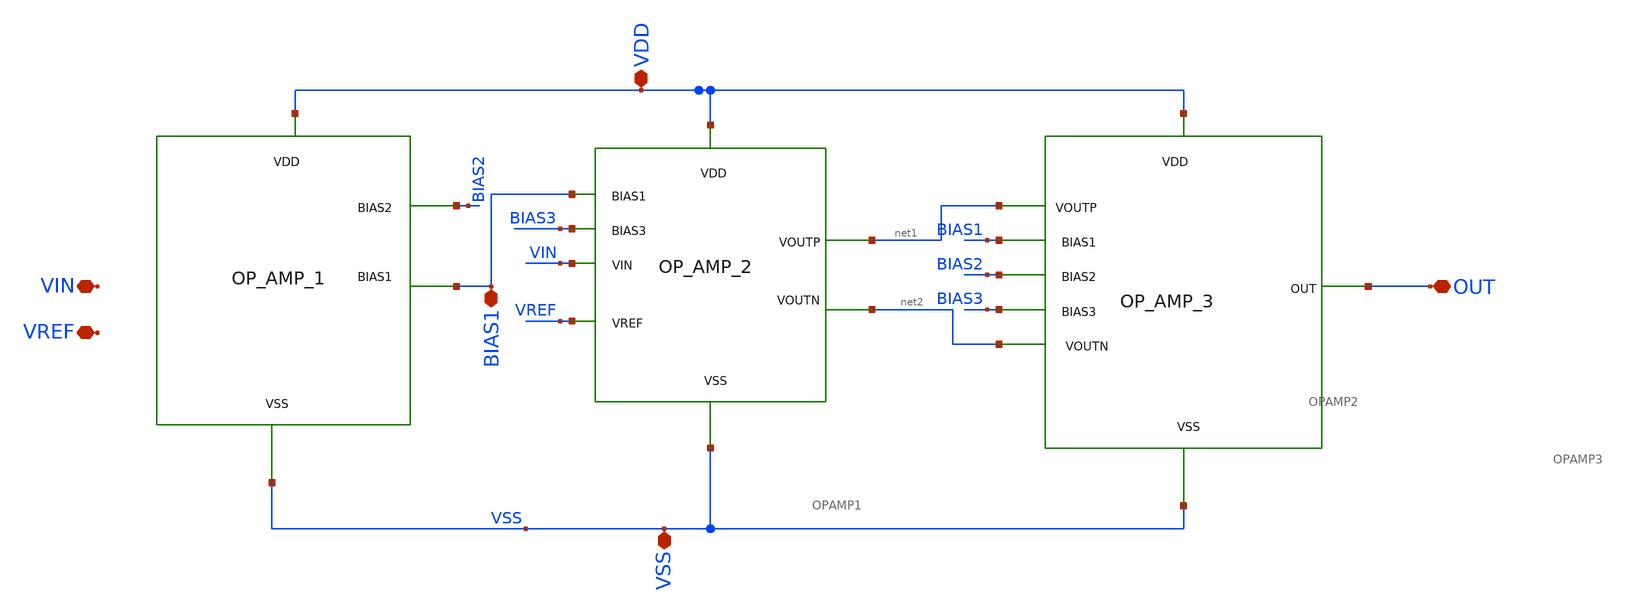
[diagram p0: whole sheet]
** sch_path: xschem/DC_DC_Converter_xschem/OPAMP_Blocks.sch
**.subckt OPAMP_Blocks VDD VSS BIAS1 VIN OUT VREF
*.iopin VDD
*.iopin VSS
*.iopin BIAS1
*.iopin VIN
*.iopin OUT
*.iopin VREF
x1 BIAS1 VDD VSS BIAS2 OPAMP1
x2 VDD BIAS1 net1 net2 VIN VREF VSS BIAS3 OPAMP2
x3 VDD net1 net2 OUT VSS BIAS1 BIAS2 BIAS3 OPAMP3
**.ends
.end
